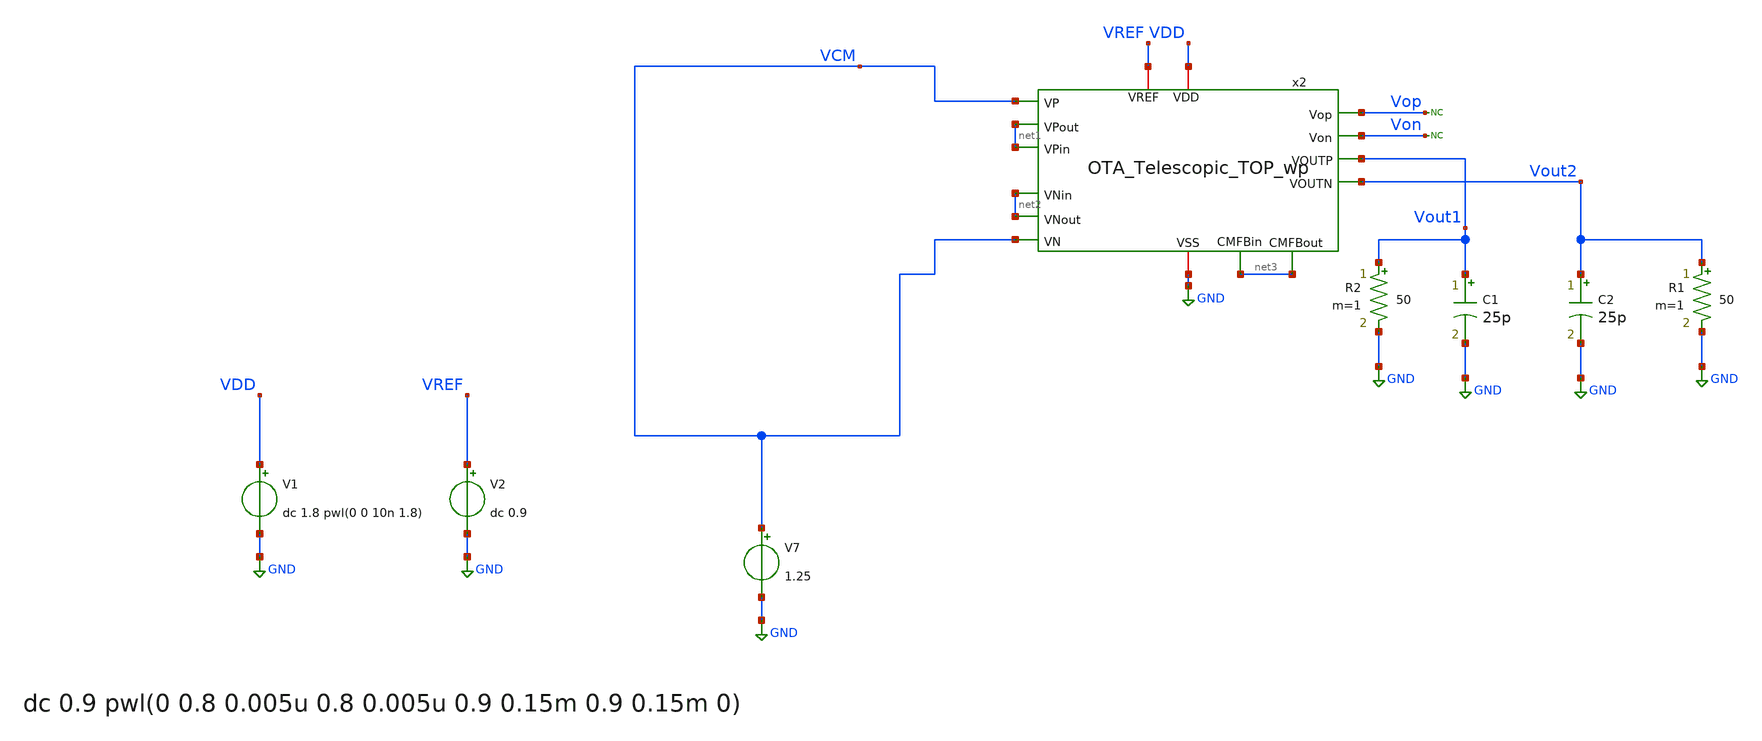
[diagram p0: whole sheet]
** sch_path: OTA_Telescopic_NO_FLATTEN/Testbenchs/OTA_Telescopic_TOP_TB_StartUp.sch
**.subckt OTA_Telescopic_TOP_TB_StartUp
V7 VCM GND 1.25
V1 VDD GND dc 1.8 pwl(0 0 10n 1.8)
V2 VREF GND dc 0.9
C1 Vout1 GND 25p m=1
C2 Vout2 GND 25p m=1
x2 VDD GND net1 net1 Vout1 VCM VCM Vout2 net2 net2 net3 VREF net3 Vop Von OTA_Telescopic_TOP_wp
R1 Vout2 GND 50 m=1
R2 Vout1 GND 50 m=1
* noconn Vop
* noconn Von
**** begin user architecture code

** opencircuitdesign pdks install
.lib cornerMOSlv.lib mos_tt
.lib cornerRES.lib res_typ
.lib cornerCAP.lib cap_typ
.temp 65




.control
 set color0 = white

set wr_singlescale
set wr_vecnames

save all
tran 10p 500n
*write NMOS_diode_large_signal.raw

let VCM = v(Vout1)
let VDD = v(VDD)
let IDD = -i(V1)

*wrdata VCM_ss_10ns_DC.txt VCM
*wrdata IDD_ss_10ns_DC.txt IDD

plot VCM
plot VDD
plot IDD

let Vo1 = v(x1.Vo1)
let Vo2 = v(x1.Vo2)

let Vo = Vo1-Vo2

wrdata Vo Vo

reset
noise v(Vout1) V5 dec 100 1 0.5e9 1
setplot noise1
*plot onoise_spectrum
setplot noise2
print onoise_total

.endc


**** end user architecture code
**.ends
.GLOBAL GND
.end
